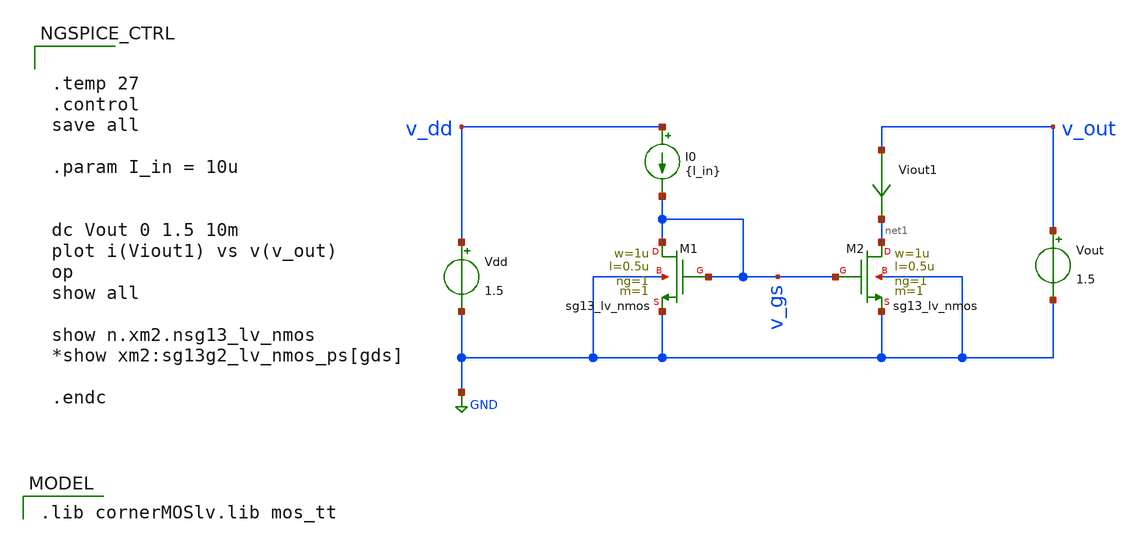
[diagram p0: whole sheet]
** sch_path: assignment_1_task_2.sch
**.subckt assignment_1_task_2
XM1 v_gs v_gs GND GND sg13_lv_nmos w=1u l=0.5u ng=1 m=1 mm_ok=1
XM2 net1 v_gs GND GND sg13_lv_nmos w=1u l=0.5u ng=1 m=1 mm_ok=1
Vdd v_dd GND 1.5
I0 v_dd v_gs {I_in}
Vout v_out GND 1.5
Viout1 v_out net1 0
.save i(viout1)
**** begin user architecture code


.temp 27
.control
save all

.param I_in = 10u


dc Vout 0 1.5 10m
plot i(Viout1) vs v(v_out)
op
show all

show n.xm2.nsg13_lv_nmos
*show xm2:sg13g2_lv_nmos_ps[gds]

.endc


 .lib cornerMOSlv.lib mos_tt

**** end user architecture code
**.ends
.GLOBAL GND
.end
